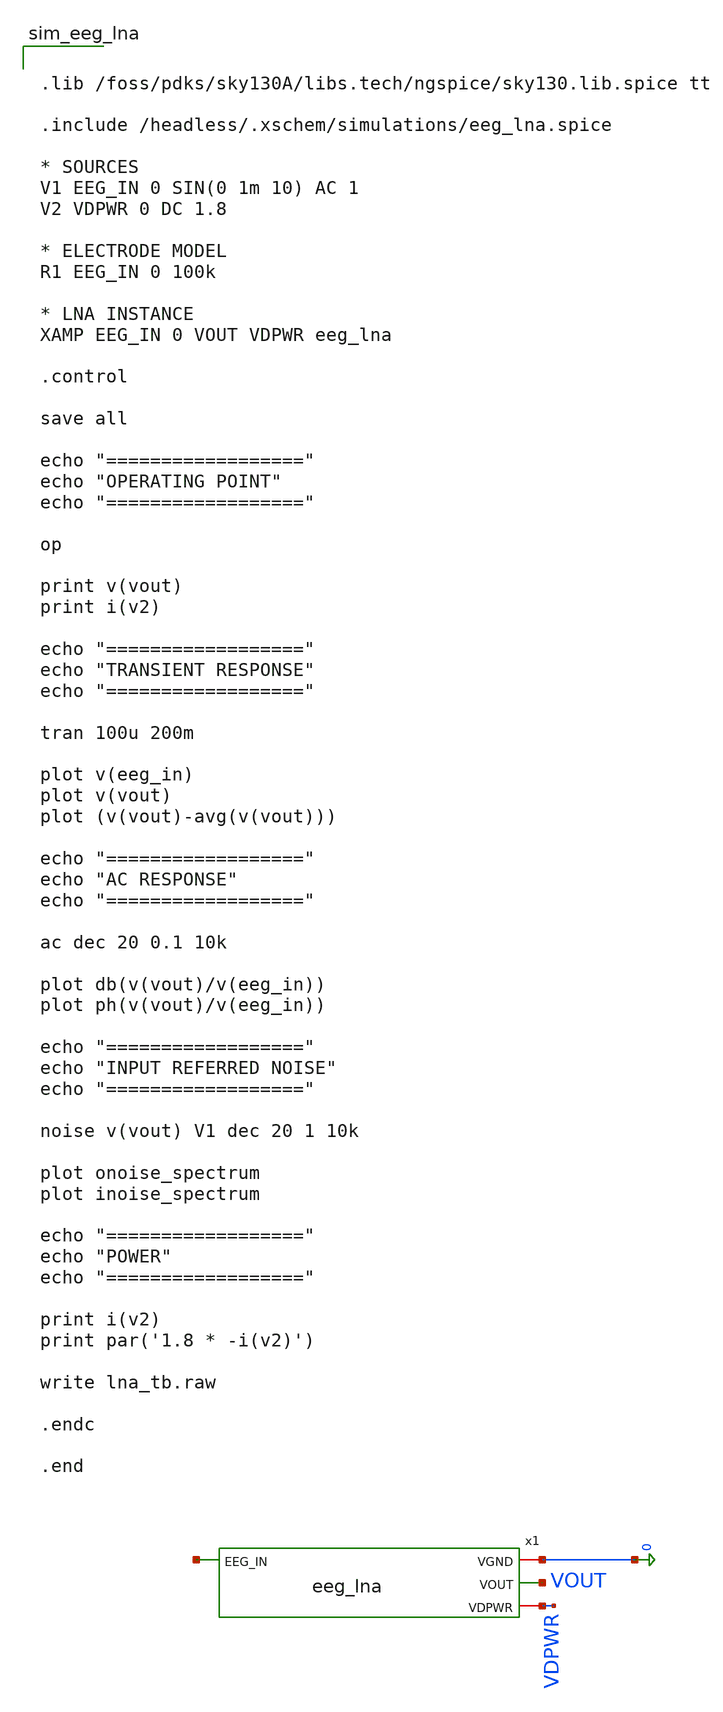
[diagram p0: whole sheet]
** sch_path: xschem/eeg_lna_tb.sch
**.subckt eeg_lna_tb
x1 net1 0 VOUT VDPWR eeg_lna
**** begin user architecture code


.lib /foss/pdks/sky130A/libs.tech/ngspice/sky130.lib.spice tt

.include /headless/.xschem/simulations/eeg_lna.spice

* SOURCES
V1 EEG_IN 0 SIN(0 1m 10) AC 1
V2 VDPWR 0 DC 1.8

* ELECTRODE MODEL
R1 EEG_IN 0 100k

* LNA INSTANCE
XAMP EEG_IN 0 VOUT VDPWR eeg_lna

.control

save all

echo "=================="
echo "OPERATING POINT"
echo "=================="

op

print v(vout)
print i(v2)

echo "=================="
echo "TRANSIENT RESPONSE"
echo "=================="

tran 100u 200m

plot v(eeg_in)
plot v(vout)
plot (v(vout)-avg(v(vout)))

echo "=================="
echo "AC RESPONSE"
echo "=================="

ac dec 20 0.1 10k

plot db(v(vout)/v(eeg_in))
plot ph(v(vout)/v(eeg_in))

echo "=================="
echo "INPUT REFERRED NOISE"
echo "=================="

noise v(vout) V1 dec 20 1 10k

plot onoise_spectrum
plot inoise_spectrum

echo "=================="
echo "POWER"
echo "=================="

print i(v2)
print par('1.8 * -i(v2)')

write lna_tb.raw

.endc

.end


**** end user architecture code
**.ends

* expanding   symbol:  eeg_lna.sym # of pins=4
** sym_path: xschem/eeg_lna.sym
** sch_path: xschem/eeg_lna.sch
.subckt eeg_lna EEG_IN VGND VOUT VDPWR
*.iopin VGND
*.ipin EEG_IN
*.iopin VDPWR
*.opin VOUT
XM1 MIRROR_BIAS_N MIRROR_BIAS_N VGND VGND sky130_fd_pr__nfet_01v8 L=1.0 W=4 nf=1 ad='int((1 + 1)/2) * 4 / 1 * 0.29'
+ as='int((1 + 2)/2) * 4 / 1 * 0.29' pd='2*int((1 + 1)/2) * (4 / 1 + 0.29)' ps='2*int((1 + 2)/2) * (4 / 1 + 0.29)'
+ nrd='0.29 / 4 ' nrs='0.29 / 4 ' sa=0 sb=0 sd=0 mult=1 m=1
XM2 VOUT MIRROR_BIAS_N VGND VGND sky130_fd_pr__nfet_01v8 L=1.0 W=4 nf=1 ad='int((1 + 1)/2) * 4 / 1 * 0.29'
+ as='int((1 + 2)/2) * 4 / 1 * 0.29' pd='2*int((1 + 1)/2) * (4 / 1 + 0.29)' ps='2*int((1 + 2)/2) * (4 / 1 + 0.29)'
+ nrd='0.29 / 4 ' nrs='0.29 / 4 ' sa=0 sb=0 sd=0 mult=1 m=1
XM3 MIRROR_BIAS_N VIN_P TAIL_P VDPWR sky130_fd_pr__pfet_01v8 L=1.0 W=8 nf=1 ad='int((1 + 1)/2) * 8 / 1 * 0.29'
+ as='int((1 + 2)/2) * 8 / 1 * 0.29' pd='2*int((1 + 1)/2) * (8 / 1 + 0.29)' ps='2*int((1 + 2)/2) * (8 / 1 + 0.29)'
+ nrd='0.29 / 8 ' nrs='0.29 / 8 ' sa=0 sb=0 sd=0 mult=1 m=1
XM4 VOUT VIN_N TAIL_P VDPWR sky130_fd_pr__pfet_01v8 L=1.0 W=8 nf=1 ad='int((1 + 1)/2) * 8 / 1 * 0.29'
+ as='int((1 + 2)/2) * 8 / 1 * 0.29' pd='2*int((1 + 1)/2) * (8 / 1 + 0.29)' ps='2*int((1 + 2)/2) * (8 / 1 + 0.29)'
+ nrd='0.29 / 8 ' nrs='0.29 / 8 ' sa=0 sb=0 sd=0 mult=1 m=1
XM5 TAIL_P BIAS_P VDPWR VDPWR sky130_fd_pr__pfet_01v8 L=1.0 W=8 nf=1 ad='int((1 + 1)/2) * 8 / 1 * 0.29'
+ as='int((1 + 2)/2) * 8 / 1 * 0.29' pd='2*int((1 + 1)/2) * (8 / 1 + 0.29)' ps='2*int((1 + 2)/2) * (8 / 1 + 0.29)'
+ nrd='0.29 / 8 ' nrs='0.29 / 8 ' sa=0 sb=0 sd=0 mult=1 m=1
XM6 BIAS_P BIAS_P VDPWR VDPWR sky130_fd_pr__pfet_01v8 L=1.0 W=4 nf=1 ad='int((1 + 1)/2) * 4 / 1 * 0.29'
+ as='int((1 + 2)/2) * 4 / 1 * 0.29' pd='2*int((1 + 1)/2) * (4 / 1 + 0.29)' ps='2*int((1 + 2)/2) * (4 / 1 + 0.29)'
+ nrd='0.29 / 4 ' nrs='0.29 / 4 ' sa=0 sb=0 sd=0 mult=1 m=1
XM7 BIAS_P BIAS_P VGND VGND sky130_fd_pr__nfet_01v8 L=1.0 W=2 nf=1 ad='int((1 + 1)/2) * 2 / 1 * 0.29'
+ as='int((1 + 2)/2) * 2 / 1 * 0.29' pd='2*int((1 + 1)/2) * (2 / 1 + 0.29)' ps='2*int((1 + 2)/2) * (2 / 1 + 0.29)'
+ nrd='0.29 / 2 ' nrs='0.29 / 2 ' sa=0 sb=0 sd=0 mult=1 m=1
XCIN VIN_P EEG_IN sky130_fd_pr__cap_mim_m3_1 W=20 L=20 MF=1 m=1
RBIAS VIN_P BIAS_P 1Gig m=1
RF VOUT VIN_N 1Meg m=1
RG VIN_N BIAS_P 100k m=1
.ends

.end
